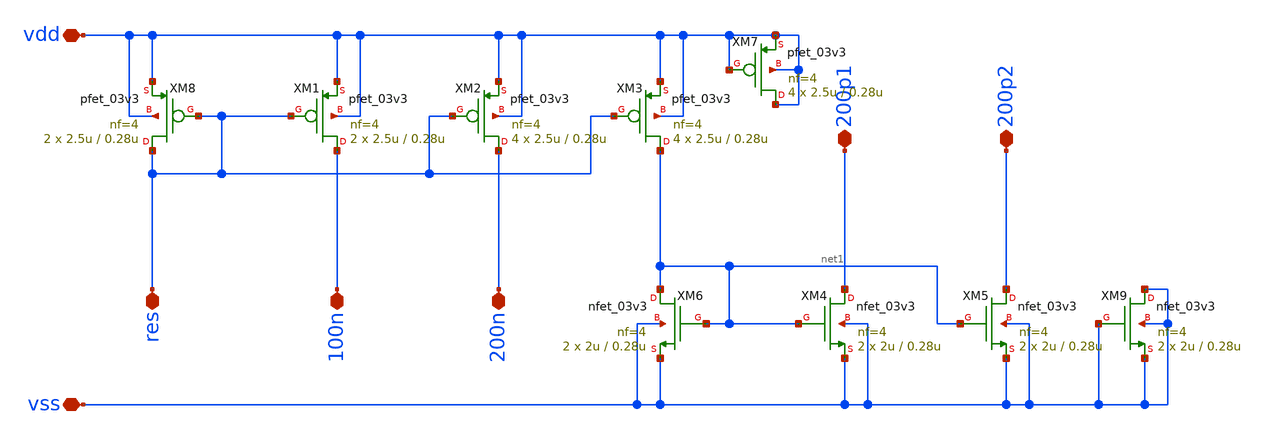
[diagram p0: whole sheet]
** sch_path: designs/libs/qw_core_analog/BIAS/BIAS.sch
**.subckt BIAS res 100n 200n 200p1 200p2 vdd vss
*.iopin res
*.iopin 100n
*.iopin 200n
*.iopin 200p1
*.iopin 200p2
*.iopin vdd
*.iopin vss
XM8 res res vdd vdd pfet_03v3 L=0.28u W=2.5u nf=4 ad='int((nf+1)/2) * W/nf * 0.18u' as='int((nf+2)/2) * W/nf * 0.18u'
+ pd='2*int((nf+1)/2) * (W/nf + 0.18u)' ps='2*int((nf+2)/2) * (W/nf + 0.18u)' nrd='0.18u / W' nrs='0.18u / W'
+ sa=0 sb=0 sd=0 m=2
XM1 100n res vdd vdd pfet_03v3 L=0.28u W=2.5u nf=4 ad='int((nf+1)/2) * W/nf * 0.18u' as='int((nf+2)/2) * W/nf * 0.18u'
+ pd='2*int((nf+1)/2) * (W/nf + 0.18u)' ps='2*int((nf+2)/2) * (W/nf + 0.18u)' nrd='0.18u / W' nrs='0.18u / W'
+ sa=0 sb=0 sd=0 m=2
XM2 200n res vdd vdd pfet_03v3 L=0.28u W=2.5u nf=4 ad='int((nf+1)/2) * W/nf * 0.18u' as='int((nf+2)/2) * W/nf * 0.18u'
+ pd='2*int((nf+1)/2) * (W/nf + 0.18u)' ps='2*int((nf+2)/2) * (W/nf + 0.18u)' nrd='0.18u / W' nrs='0.18u / W'
+ sa=0 sb=0 sd=0 m=4
XM3 net1 res vdd vdd pfet_03v3 L=0.28u W=2.5u nf=4 ad='int((nf+1)/2) * W/nf * 0.18u' as='int((nf+2)/2) * W/nf * 0.18u'
+ pd='2*int((nf+1)/2) * (W/nf + 0.18u)' ps='2*int((nf+2)/2) * (W/nf + 0.18u)' nrd='0.18u / W' nrs='0.18u / W'
+ sa=0 sb=0 sd=0 m=4
XM6 net1 net1 vss vss nfet_03v3 L=0.28u W=2u nf=4 ad='int((nf+1)/2) * W/nf * 0.18u' as='int((nf+2)/2) * W/nf * 0.18u'
+ pd='2*int((nf+1)/2) * (W/nf + 0.18u)' ps='2*int((nf+2)/2) * (W/nf + 0.18u)' nrd='0.18u / W' nrs='0.18u / W'
+ sa=0 sb=0 sd=0 m=2
XM4 200p1 net1 vss vss nfet_03v3 L=0.28u W=2u nf=4 ad='int((nf+1)/2) * W/nf * 0.18u' as='int((nf+2)/2) * W/nf * 0.18u'
+ pd='2*int((nf+1)/2) * (W/nf + 0.18u)' ps='2*int((nf+2)/2) * (W/nf + 0.18u)' nrd='0.18u / W' nrs='0.18u / W'
+ sa=0 sb=0 sd=0 m=2
XM5 200p2 net1 vss vss nfet_03v3 L=0.28u W=2u nf=4 ad='int((nf+1)/2) * W/nf * 0.18u' as='int((nf+2)/2) * W/nf * 0.18u'
+ pd='2*int((nf+1)/2) * (W/nf + 0.18u)' ps='2*int((nf+2)/2) * (W/nf + 0.18u)' nrd='0.18u / W' nrs='0.18u / W'
+ sa=0 sb=0 sd=0 m=2
XM7 vdd vdd vdd vdd pfet_03v3 L=0.28u W=2.5u nf=4 ad='int((nf+1)/2) * W/nf * 0.18u' as='int((nf+2)/2) * W/nf * 0.18u'
+ pd='2*int((nf+1)/2) * (W/nf + 0.18u)' ps='2*int((nf+2)/2) * (W/nf + 0.18u)' nrd='0.18u / W' nrs='0.18u / W'
+ sa=0 sb=0 sd=0 m=4
XM9 vss vss vss vss nfet_03v3 L=0.28u W=2u nf=4 ad='int((nf+1)/2) * W/nf * 0.18u' as='int((nf+2)/2) * W/nf * 0.18u'
+ pd='2*int((nf+1)/2) * (W/nf + 0.18u)' ps='2*int((nf+2)/2) * (W/nf + 0.18u)' nrd='0.18u / W' nrs='0.18u / W'
+ sa=0 sb=0 sd=0 m=2
**.ends
.end
